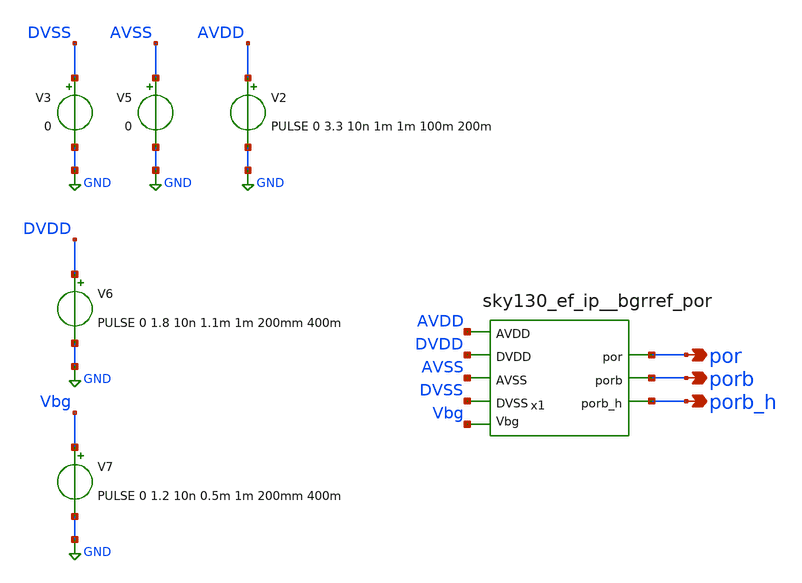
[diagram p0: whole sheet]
** sch_path: xschem/sky130_ef_ip__bgrref_por_tb1.sch
**.subckt sky130_ef_ip__bgrref_por_tb1 por porb porb_h
*.opin por
*.opin porb
*.opin porb_h
x1 Vbg por AVSS AVDD DVDD porb DVSS porb_h VCC VSS sky130_ef_ip__bgrref_por W_N=1 L_N=0.2 W_P=1
+ L_P=0.2 m=1
V3 DVSS GND 0
V2 AVDD GND PULSE 0 3.3 10n 1m 1m 100m 200m
V5 AVSS GND 0
V6 DVDD GND PULSE 0 1.8 10n 1.1m 1m 200mm 400m
V7 Vbg GND PULSE 0 1.2 10n 0.5m 1m 200mm 400m
**** begin user architecture code
 .lib $::SKYWATER_MODELS/sky130.lib.spice tt

.include $::SKYWATER_STDCELLS/sky130_fd_sc_hd.spice
.include /foss/pdks/sky130A/libs.ref/sky130_fd_sc_hvl/spice/sky130_fd_sc_hvl.spice




.option method=gear
.options savecurrents
.control
save all
set temp=-40
tran .1u 2m
plot AVDD por porb+6.8 porb_h+3.4
write sky130_ef_ip__bgrref_por_tb1.raw

set appendwrite
set temp=27
tran .1u 2m
write sky130_ef_ip__bgrref_por_tb1.raw

set appendwrite
set temp=85
tran .1u 2m
write sky130_ef_ip__bgrref_por_tb1.raw

*quit 0
.endc


**** end user architecture code
**.ends
.GLOBAL GND
.end
